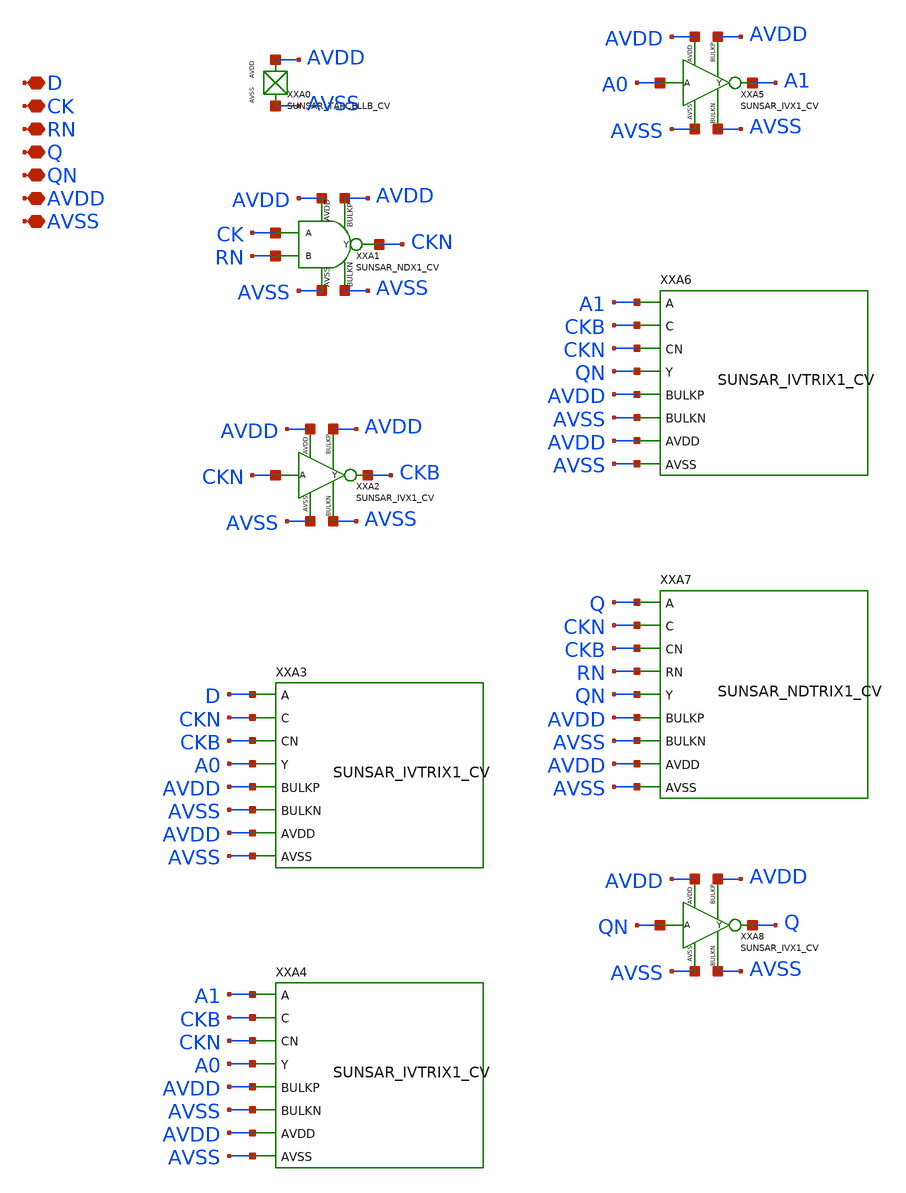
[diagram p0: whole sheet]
** sch_path: design/SUN_SAR9B_SKY130NM/SUNSAR_DFRNQNX1_CV.sch
**.subckt SUNSAR_DFRNQNX1_CV D CK RN Q QN AVDD AVSS
*.iopin D
*.iopin CK
*.iopin RN
*.iopin Q
*.iopin QN
*.iopin AVDD
*.iopin AVSS
XXA0 AVDD AVSS SUNSAR_TAPCELLB_CV
XXA1 CK RN CKN AVDD AVSS AVDD AVSS SUNSAR_NDX1_CV
XXA2 CKN CKB AVDD AVSS AVDD AVSS SUNSAR_IVX1_CV
XXA3 D CKN CKB A0 AVDD AVSS AVDD AVSS SUNSAR_IVTRIX1_CV
XXA4 A1 CKB CKN A0 AVDD AVSS AVDD AVSS SUNSAR_IVTRIX1_CV
XXA5 A0 A1 AVDD AVSS AVDD AVSS SUNSAR_IVX1_CV
XXA6 A1 CKB CKN QN AVDD AVSS AVDD AVSS SUNSAR_IVTRIX1_CV
XXA7 Q CKN CKB RN QN AVDD AVSS AVDD AVSS SUNSAR_NDTRIX1_CV
XXA8 QN Q AVDD AVSS AVDD AVSS SUNSAR_IVX1_CV
**.ends
.end
